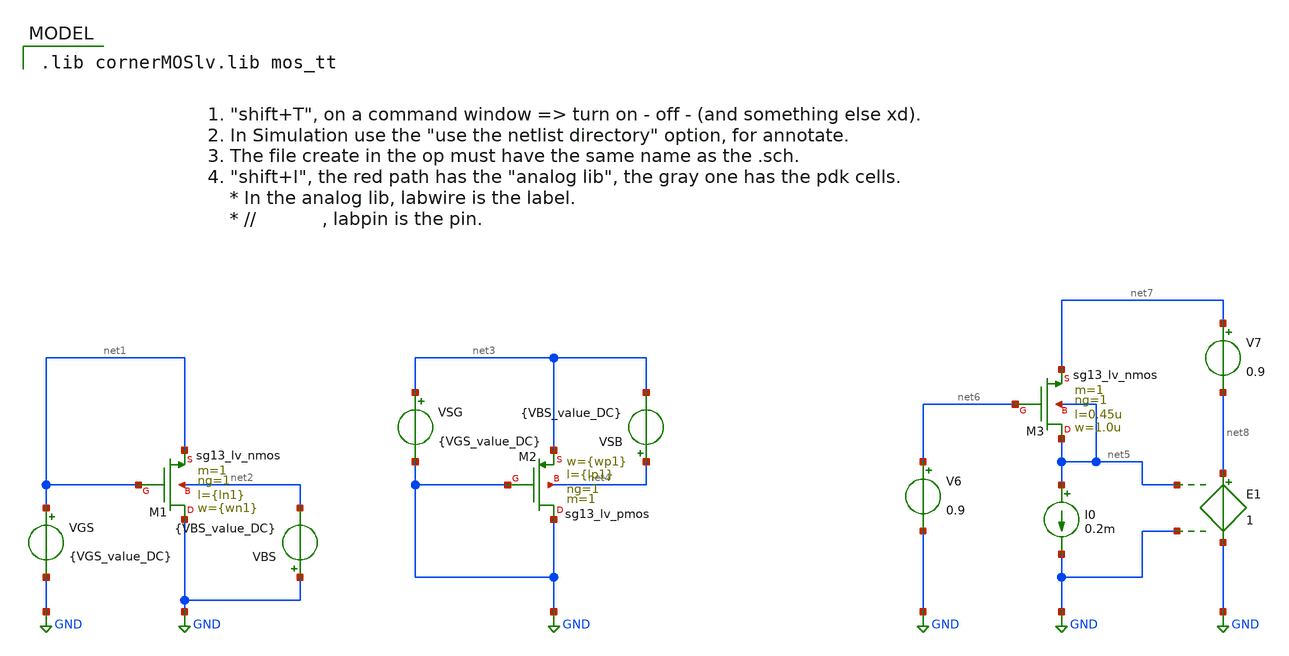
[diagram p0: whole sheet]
** sch_path: W2WDAC/W2W-DAC/CMOSCHART_sg130_lv_diode_tb.sch
**.subckt CMOSCHART_sg130_lv_diode_tb
VGS net1 GND {VGS_value_DC}
VBS GND net2 {VBS_value_DC}
VSG net3 GND {VGS_value_DC}
VSB net4 net3 {VBS_value_DC}
I0 net5 GND 0.2m
V6 net6 GND 0.9
V7 net7 net8 0.9
E1 net8 GND net5 GND 1
XM1 GND net1 net1 net2 sg13_lv_nmos w={wn1} l={ln1} ng=1 m=1 mm_ok=1
XM2 GND GND net3 net4 sg13_lv_pmos w={wp1} l={lp1} ng=1 m=1 mm_ok=1
XM3 net5 net6 net7 net5 sg13_lv_nmos w=1.0u l=0.45u ng=1 m=1 mm_ok=1
**** begin user architecture code



.op
.save all
.control

run
let Vgsn = @n.xm1.nsg13_lv_nmos[vgs]
let Vdsn = @n.xm1.nsg13_lv_nmos[vds]
let idn = @n.xm1.nsg13_lv_nmos[ids]
let gmn = @n.xm1.nsg13_lv_nmos[gm]
let vdsatn = @n.xm1.nsg13_lv_nmos[vsat]
let vthn = @n.xm1.nsg13_lv_nmos[vth]
let ron = @n.xm1.nsg13_lv_nmos[gds]
let cggn = @n.xm1.nsg13_lv_nmos[cgg]
let gm_idn = gmn/idn
let ftn = gmn / (6.283 * cggn)
let ftgm_idn = ftn * (gmn/idn)
let aon = gmn*ron
let Vovn = Vgsn - vthn
let deltaVdsn = Vdsn - vdsatn

print Vgsn Vdsn idn vdsatn vthn deltaVdsn Vovn gmn ron cggn gm_idn ftn ftgm_idn aon

write CMOSCHART_sg130_lv_tb.raw
set appendwrite


.endc


 .lib cornerMOSlv.lib mos_tt



.temp 65
.param wn1=0.3u
.param ln1=0.39u
.param wp1=3.235u
.param lp1=0.39u
.param VGS_value_DC=0.6
.param VBS_value_DC=0



**** end user architecture code
**.ends
.GLOBAL GND
.end
